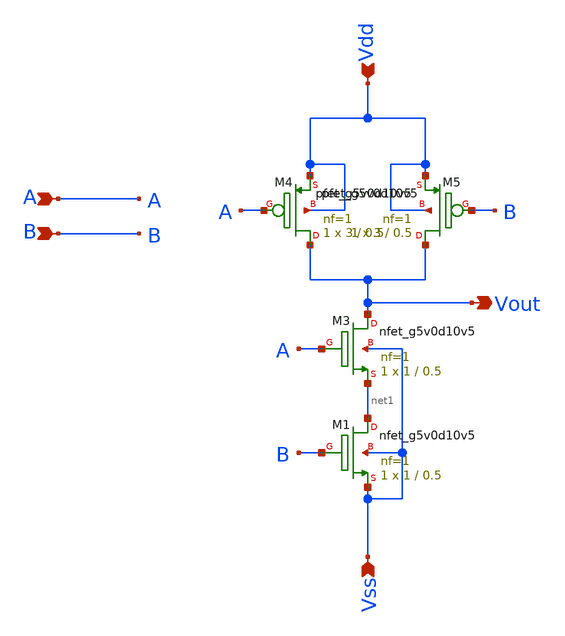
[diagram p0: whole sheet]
** sch_path: xschem/NAND_GATE.sch
**.subckt NAND_GATE Vdd Vss A B Vout
*.ipin Vdd
*.ipin Vss
*.ipin A
*.ipin B
*.opin Vout
XM3 Vout A net1 Vss sky130_fd_pr__nfet_g5v0d10v5 L=0.5 W=1 nf=1 ad='int((1 + 1)/2) * 1 / 1 * 0.29' as='int((1 + 2)/2) * 1 / 1 * 0.29'
+ pd='2*int((1 + 1)/2) * (1 / 1 + 0.29)' ps='2*int((1 + 2)/2) * (1 / 1 + 0.29)' nrd='0.29 / 1 ' nrs='0.29 / 1 '
+ sa=0 sb=0 sd=0 mult=1 m=1
XM4 Vout A Vdd Vdd sky130_fd_pr__pfet_g5v0d10v5 L=0.5 W=3 nf=1 ad='int((1 + 1)/2) * 3 / 1 * 0.29' as='int((1 + 2)/2) * 3 / 1 * 0.29'
+ pd='2*int((1 + 1)/2) * (3 / 1 + 0.29)' ps='2*int((1 + 2)/2) * (3 / 1 + 0.29)' nrd='0.29 / 3 ' nrs='0.29 / 3 '
+ sa=0 sb=0 sd=0 mult=1 m=1
XM5 Vout B Vdd Vdd sky130_fd_pr__pfet_g5v0d10v5 L=0.5 W=3 nf=1 ad='int((1 + 1)/2) * 3 / 1 * 0.29' as='int((1 + 2)/2) * 3 / 1 * 0.29'
+ pd='2*int((1 + 1)/2) * (3 / 1 + 0.29)' ps='2*int((1 + 2)/2) * (3 / 1 + 0.29)' nrd='0.29 / 3 ' nrs='0.29 / 3 '
+ sa=0 sb=0 sd=0 mult=1 m=1
XM1 net1 B Vss Vss sky130_fd_pr__nfet_g5v0d10v5 L=0.5 W=1 nf=1 ad='int((1 + 1)/2) * 1 / 1 * 0.29' as='int((1 + 2)/2) * 1 / 1 * 0.29'
+ pd='2*int((1 + 1)/2) * (1 / 1 + 0.29)' ps='2*int((1 + 2)/2) * (1 / 1 + 0.29)' nrd='0.29 / 1 ' nrs='0.29 / 1 '
+ sa=0 sb=0 sd=0 mult=1 m=1
**.ends
.end
